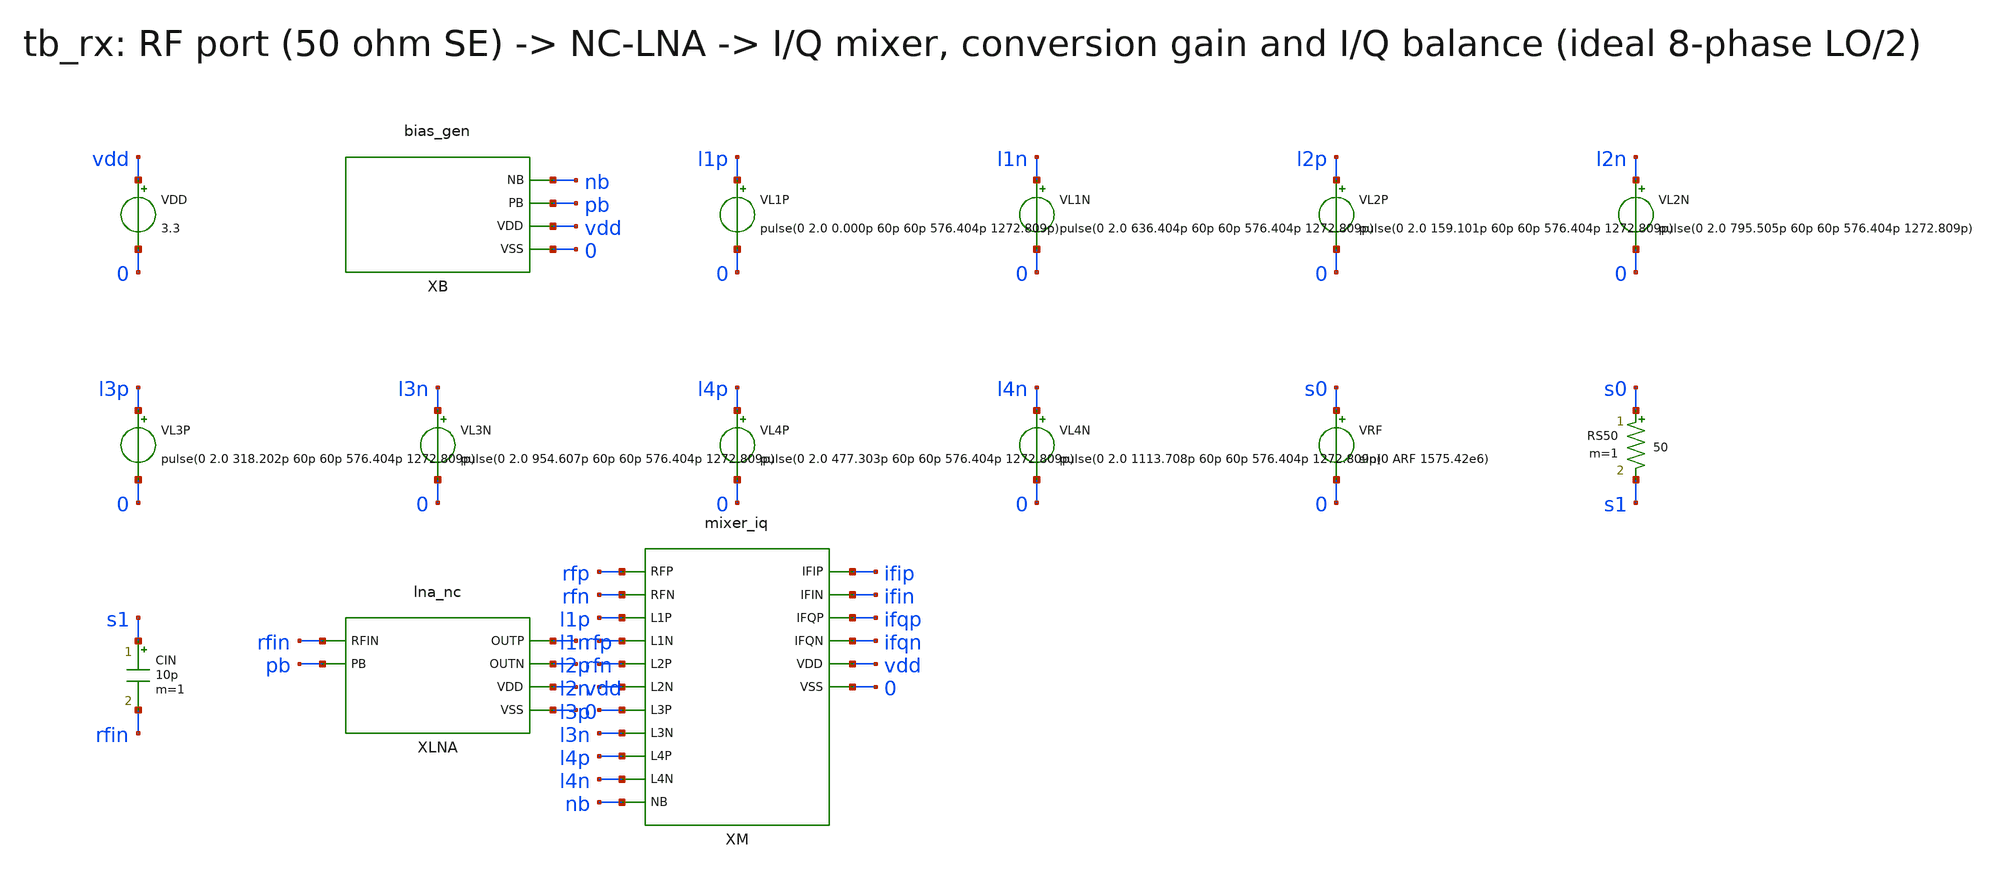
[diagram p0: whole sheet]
** sch_path: v1_claude/xschem/tb_rx.sch
**.subckt tb_rx
VDD vdd 0 3.3
XB nb pb vdd 0 bias_gen
VL1P l1p 0 pulse(0 2.0 0.000p 60p 60p 576.404p 1272.809p)
VL1N l1n 0 pulse(0 2.0 636.404p 60p 60p 576.404p 1272.809p)
VL2P l2p 0 pulse(0 2.0 159.101p 60p 60p 576.404p 1272.809p)
VL2N l2n 0 pulse(0 2.0 795.505p 60p 60p 576.404p 1272.809p)
VL3P l3p 0 pulse(0 2.0 318.202p 60p 60p 576.404p 1272.809p)
VL3N l3n 0 pulse(0 2.0 954.607p 60p 60p 576.404p 1272.809p)
VL4P l4p 0 pulse(0 2.0 477.303p 60p 60p 576.404p 1272.809p)
VL4N l4n 0 pulse(0 2.0 1113.708p 60p 60p 576.404p 1272.809p)
VRF s0 0 sin(0 ARF 1575.42e6)
RS50 s0 s1 50 m=1
CIN s1 rfin 10p m=1
XLNA rfin pb rfp rfn vdd 0 lna_nc
XM rfp rfn l1p l1n l2p l2n l3p l3n l4p l4n nb ifip ifin ifqp ifqn vdd 0 mixer_iq
**** begin user architecture code
 .include $::180MCU_MODELS/design.ngspice
.lib $::180MCU_MODELS/sm141064.ngspice typical
.lib $::180MCU_MODELS/sm141064.ngspice res_typical
.lib $::180MCU_MODELS/sm141064.ngspice mimcap_typical

.option method=gear
.control
set num_threads=1
tran 5p 0.75u 0 5p
linearize v(ifip) v(ifin) v(ifqp) v(ifqn) v(rfin)
let vi = v(ifip)-v(ifin)
let vq = v(ifqp)-v(ifqn)
wrdata tb_rx_out vi vq v(rfin)
.endc

**** end user architecture code
**.ends
.end
